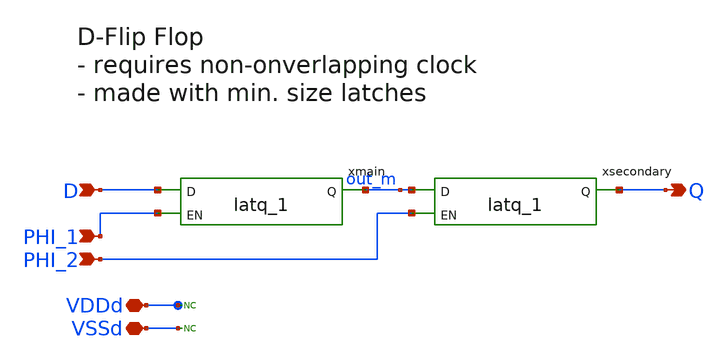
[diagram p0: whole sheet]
** sch_path: designs/switch_matrix_gf180mcu_9t5v0-main/DFF_flatten/DFF_flatten.sch
**.subckt DFF_flatten D PHI_1 PHI_2 Q VDDd VSSd
*.ipin D
*.ipin PHI_1
*.ipin PHI_2
*.opin Q
*.iopin VDDd
*.iopin VSSd
* noconn VSSd
* noconn VDDd
xmain D PHI_1 out_m VDDd VDDd VSSd VSSd gf180mcu_fd_sc_mcu9t5v0__latq_1
xsecondary out_m PHI_2 Q VDDd VDDd VSSd VSSd gf180mcu_fd_sc_mcu9t5v0__latq_1
**.ends
.end
